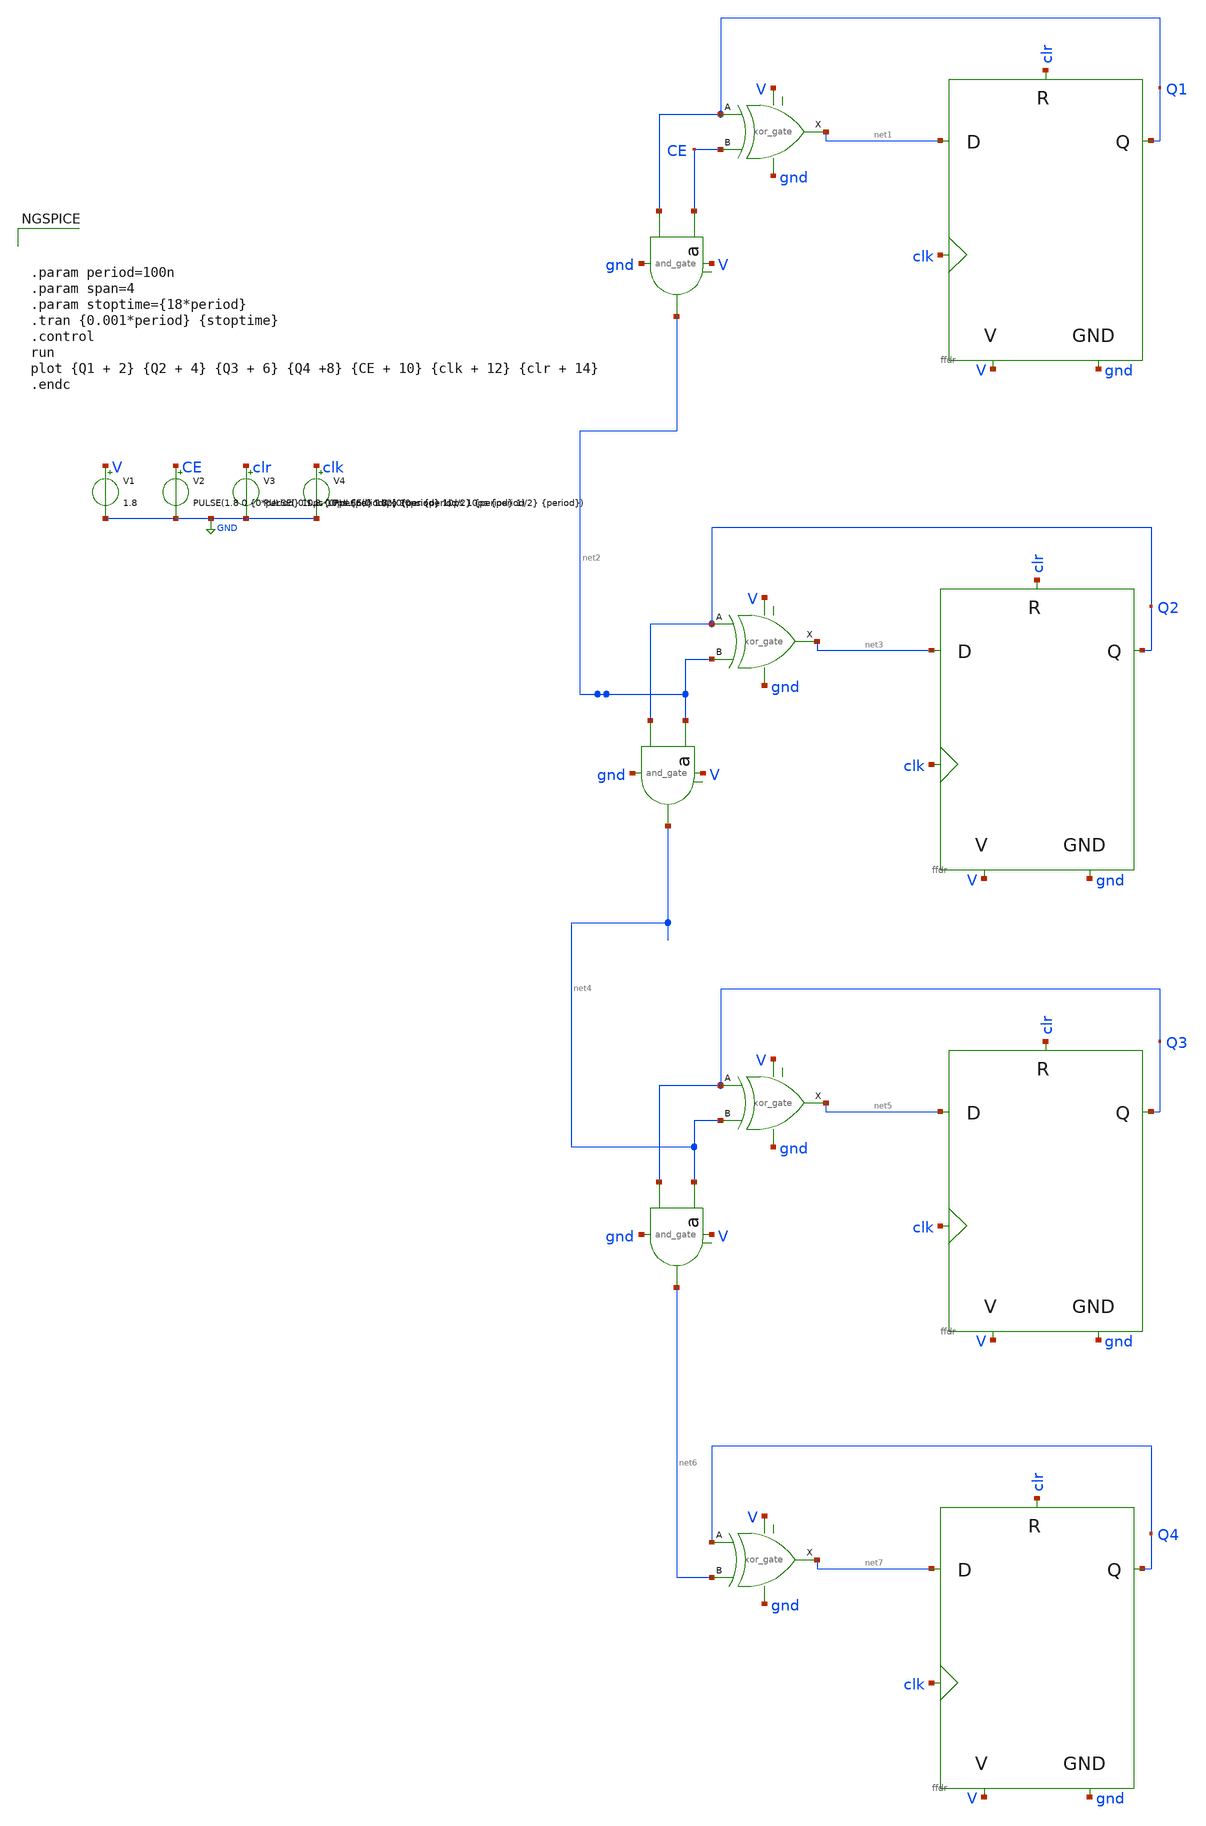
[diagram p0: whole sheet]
** sch_path: EAMTA/xschem/counter4b/symbol/counter4b.sch
**.subckt counter4b
X1 CE Q1 gnd V net2 and_gate
X2 net1 clk V gnd Q1 clr ffdr
X3 Q1 CE net1 V gnd xor_gate
X4 net2 Q2 gnd V net4 and_gate
X5 net3 clk V gnd Q2 clr ffdr
X6 Q2 net2 net3 V gnd xor_gate
X7 net4 Q3 gnd V net6 and_gate
X8 net5 clk V gnd Q3 clr ffdr
X9 Q3 net4 net5 V gnd xor_gate
X11 net7 clk V gnd Q4 clr ffdr
X12 Q4 net6 net7 V gnd xor_gate
V1 V GND 1.8
V2 CE GND PULSE(1.8 0 {0*period} 10ps 10ps {period/2} {period} 1)
V3 clr GND PULSE( 0 1.8 {0*period} 10ps 10ps {period/2} {period} 1)
V4 clk GND PULSE(0 1.8 {0*period} 10ps 10ps {period/2} {period})
**** begin user architecture code



.param period=100n
.param span=4
.param stoptime={18*period}
.tran {0.001*period} {stoptime}
.control
run
plot {Q1 + 2} {Q2 + 4} {Q3 + 6} {Q4 +8} {CE + 10} {clk + 12} {clr + 14}
.endc


.lib $env(PDK_ROOT)/$env(PDK)/libs.tech/ngspice/sky130.lib.spice.tt.red tt


**** end user architecture code
**.ends
.GLOBAL GND
.end
